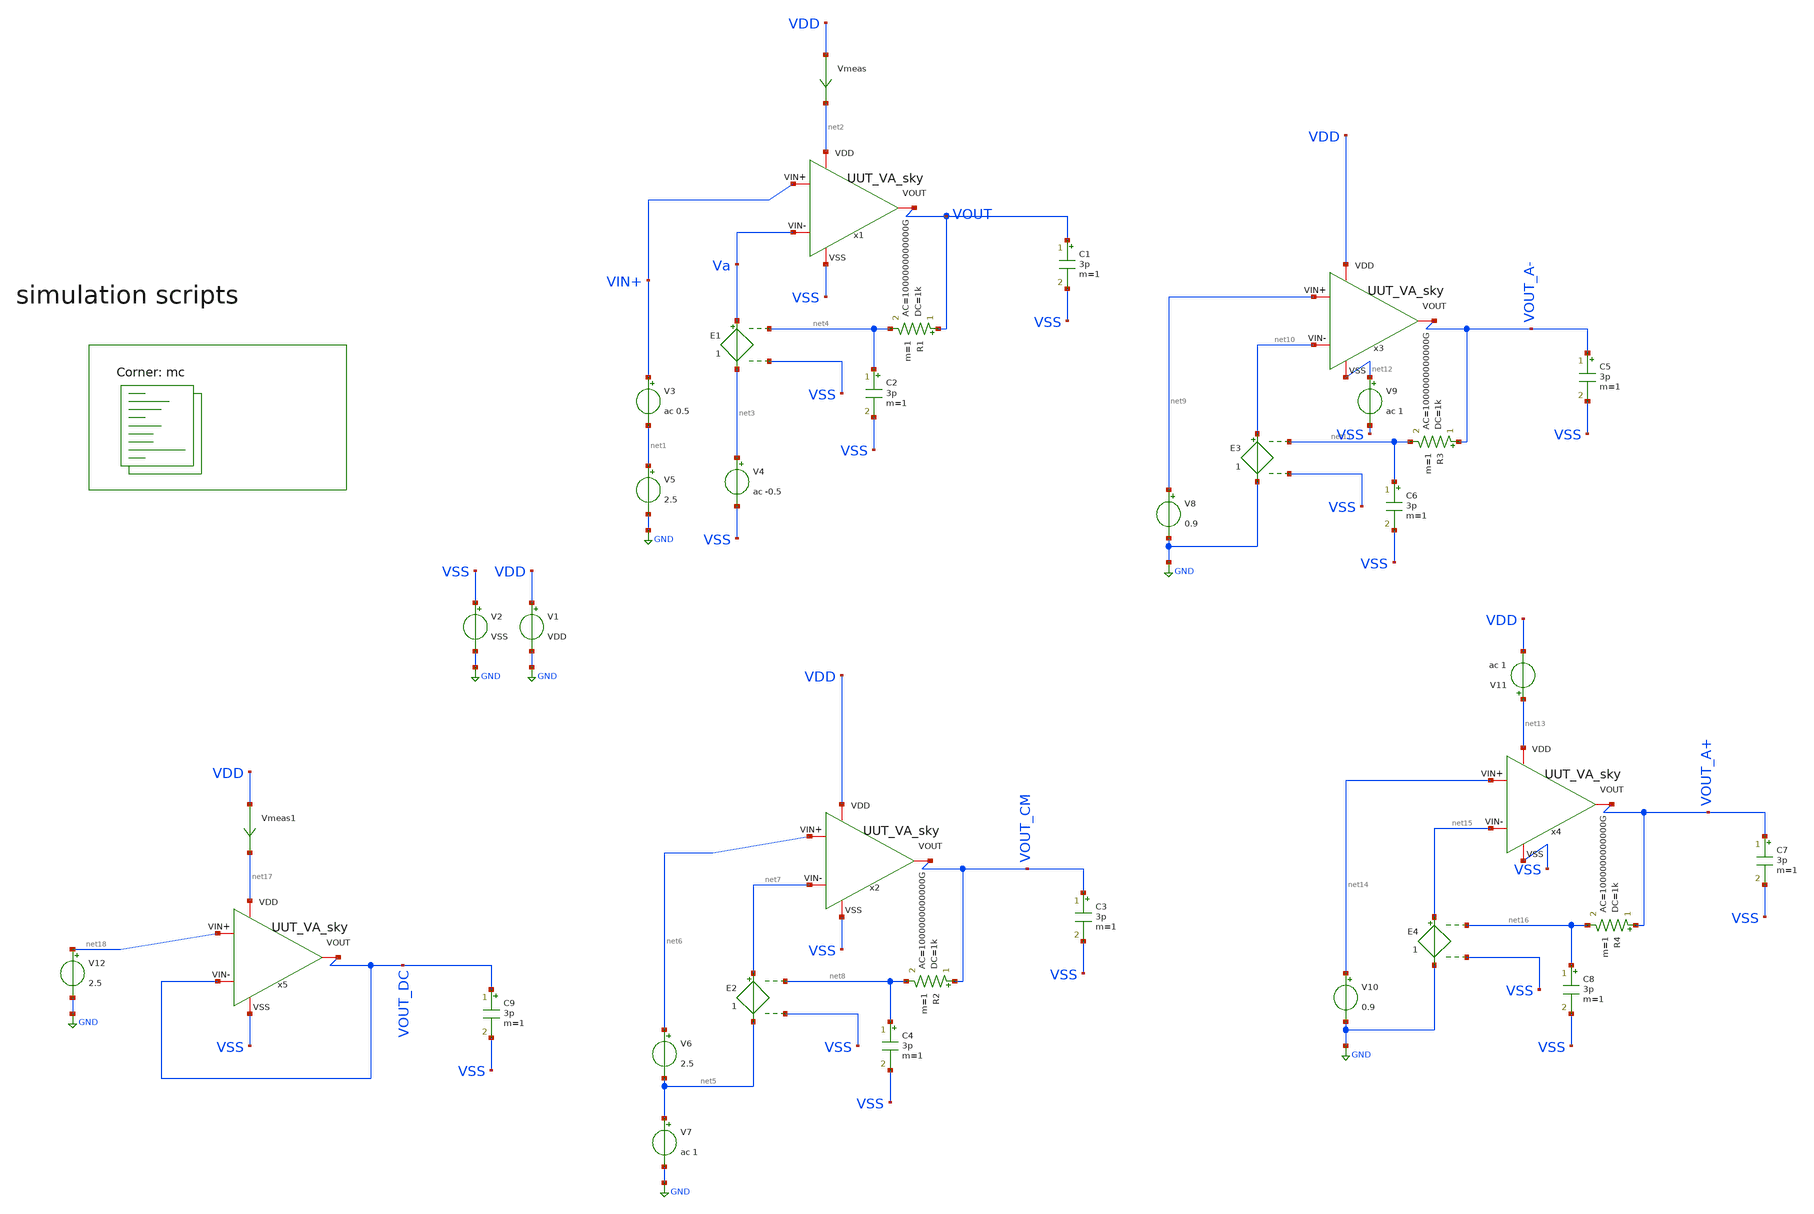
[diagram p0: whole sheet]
** sch_path: Learning/single_ended_amplifiers/Design_and_Analysis_of_Two-Stage_CMOS_Operational_Amplifier_for_Fluorescence_Signal_Processing_sky130_5V/amplifier_design/OTA_mc_tb.sch
**.subckt OTA_mc_tb
V1 VDD GND VDD
V2 VSS GND VSS
Vmeas VDD net2 0
.save i(vmeas)
x1 net2 VSS Va VIN+ VOUT UUT_VA_sky
C1 VOUT VSS 3p m=1
V5 net1 GND 2.5
V3 VIN+ net1 ac 0.5
V4 net3 VSS ac -0.5
E1 Va net3 net4 VSS 1
R1 VOUT net4 1k ac=1000000000000G m=1
C2 net4 VSS 3p m=1
x2 VDD VSS net7 net6 VOUT_CM UUT_VA_sky
C3 VOUT_CM VSS 3p m=1
V6 net6 net5 2.5
V7 net5 GND ac 1
E2 net7 net5 net8 VSS 1
R2 VOUT_CM net8 1k ac=1000000000000G m=1
C4 net8 VSS 3p m=1
x3 VDD net12 net10 net9 VOUT_A- UUT_VA_sky
C5 VOUT_A- VSS 3p m=1
V8 net9 GND 0.9
E3 net10 GND net11 VSS 1
R3 VOUT_A- net11 1k ac=1000000000000G m=1
C6 net11 VSS 3p m=1
V9 net12 VSS ac 1
x4 net13 VSS net15 net14 VOUT_A+ UUT_VA_sky
C7 VOUT_A+ VSS 3p m=1
V10 net14 GND 0.9
E4 net15 GND net16 VSS 1
R4 VOUT_A+ net16 1k ac=1000000000000G m=1
C8 net16 VSS 3p m=1
V11 net13 VDD ac 1
Vmeas1 VDD net17 0
.save i(vmeas1)
x5 net17 VSS VOUT_DC net18 VOUT_DC UUT_VA_sky
C9 VOUT_DC VSS 3p m=1
V12 net18 GND 2.5
**** begin user architecture code
.lib $::SKYWATER_MODELS/sky130.lib.spice mc

.Temp 27
.param VDD = 5
.param VSS = 0
.param CL = 3p


.control

	save all
	dc V12 0 1.8 0.001
	plot v(VOUT_DC)
	ac dec 100 1 10G
	plot db(v(VOUT))
	plot db(v(VOUT_CM))
	plot db(v(VOUT_A-))
	plot db(v(VOUT_A+))
.endc


.subckt A001 VDD VSS Vin+ Vin- VOUT
X0 bias_res_0/li_3970_7618# bias_res_0/li_2816_7756# VSS sky130_fd_pr__res_high_po_0p69 l=1.57
X1 VSS VSS VSS sky130_fd_pr__res_high_po_0p69 l=1.57
X2 bias_res_0/li_3970_7364# Lower_Nmos_0/IC VSS sky130_fd_pr__res_high_po_0p69 l=1.57
X3 bias_res_0/li_3970_7872# bias_res_0/li_2816_7756# VSS sky130_fd_pr__res_high_po_0p69 l=1.57
X4 VSS VSS VSS sky130_fd_pr__res_high_po_0p69 l=1.57
X5 bias_res_0/li_3970_8126# bias_res_0/li_2816_8248# VSS sky130_fd_pr__res_high_po_0p69 l=1.57
X6 bias_res_0/li_3969_8380# bias_res_0/li_2816_8248# VSS sky130_fd_pr__res_high_po_0p69 l=1.57
X7 VSS VSS VSS sky130_fd_pr__res_high_po_0p69 l=2.72
X8 VSS VSS VSS sky130_fd_pr__res_high_po_0p69 l=2.72
X9 bias_res_0/li_5323_7502# bias_res_0/li_3970_7364# VSS sky130_fd_pr__res_high_po_0p69 l=2.72
X10 bias_res_0/li_5323_7502# bias_res_0/li_3970_7618# VSS sky130_fd_pr__res_high_po_0p69 l=2.72
X11 bias_res_0/li_5321_8010# bias_res_0/li_3970_7872# VSS sky130_fd_pr__res_high_po_0p69 l=2.72
X12 bias_res_0/li_5321_8010# bias_res_0/li_3970_8126# VSS sky130_fd_pr__res_high_po_0p69 l=2.72
X13 VSS bias_res_0/li_3969_8380# VSS sky130_fd_pr__res_high_po_0p69 l=2.72
X14 VOUT VSS VSS VSS sky130_fd_pr__nfet_g5v0d10v5 ad=1 pd=4.5 as=1.2 ps=8.6 w=4 l=1
X15 VSS active_load_0/IA VOUT VSS sky130_fd_pr__nfet_g5v0d10v5 ad=1 pd=4.5 as=1 ps=4.5 w=4 l=1
X16 VSS VSS VOUT VSS sky130_fd_pr__nfet_g5v0d10v5 ad=1.2 pd=8.6 as=1 ps=4.5 w=4 l=1
X17 VOUT active_load_0/IA VSS VSS sky130_fd_pr__nfet_g5v0d10v5 ad=1 pd=4.5 as=1 ps=4.5 w=4 l=1
X18 VOUT VSS VSS VSS sky130_fd_pr__nfet_g5v0d10v5 ad=8 pd=36 as=20 ps=127.6 w=4 l=1
X19 VSS active_load_0/IA VOUT VSS sky130_fd_pr__nfet_g5v0d10v5 ad=0 pd=0 as=0 ps=0 w=4 l=1
X20 VSS VSS VOUT VSS sky130_fd_pr__nfet_g5v0d10v5 ad=0 pd=0 as=0 ps=0 w=4 l=1
X21 VOUT active_load_0/IA VSS VSS sky130_fd_pr__nfet_g5v0d10v5 ad=0 pd=0 as=0 ps=0 w=4 l=1
X22 VSS active_load_0/IB active_load_0/IA VSS sky130_fd_pr__nfet_g5v0d10v5 ad=0.375 pd=2 as=0.375
+ ps=2 w=1.5 l=2
X23 active_load_0/IB VSS VSS VSS sky130_fd_pr__nfet_g5v0d10v5 ad=0.375 pd=2 as=0.45 ps=3.6 w=1.5 l=2
X24 active_load_0/IA active_load_0/IB VSS VSS sky130_fd_pr__nfet_g5v0d10v5 ad=0.375 pd=2 as=0.375
+ ps=2 w=1.5 l=2
X25 VSS active_load_0/IB active_load_0/IB VSS sky130_fd_pr__nfet_g5v0d10v5 ad=0.375 pd=2 as=0.375
+ ps=2 w=1.5 l=2
X26 VSS VSS active_load_0/IB VSS sky130_fd_pr__nfet_g5v0d10v5 ad=0.45 pd=3.6 as=0.375 ps=2 w=1.5 l=2
X27 active_load_0/IB active_load_0/IB VSS VSS sky130_fd_pr__nfet_g5v0d10v5 ad=0.375 pd=2 as=0.375
+ ps=2 w=1.5 l=2
X28 VSS active_load_0/IB active_load_0/IA VSS sky130_fd_pr__nfet_g5v0d10v5 ad=0 pd=0 as=2.34 ps=14.8
+ w=1.5 l=2
X29 active_load_0/IB VSS VSS VSS sky130_fd_pr__nfet_g5v0d10v5 ad=3 pd=16 as=0 ps=0 w=1.5 l=2
X30 active_load_0/IA active_load_0/IB VSS VSS sky130_fd_pr__nfet_g5v0d10v5 ad=0 pd=0 as=0 ps=0 w=1.5
+ l=2
X31 VSS active_load_0/IB active_load_0/IB VSS sky130_fd_pr__nfet_g5v0d10v5 ad=0 pd=0 as=0 ps=0 w=1.5
+ l=2
X32 VSS VSS active_load_0/IB VSS sky130_fd_pr__nfet_g5v0d10v5 ad=0 pd=0 as=0 ps=0 w=1.5 l=2
X33 active_load_0/IB active_load_0/IB VSS VSS sky130_fd_pr__nfet_g5v0d10v5 ad=0 pd=0 as=0 ps=0 w=1.5
+ l=2
X34 active_load_0/IA Vin+ Pmos_current_mirror_0/IC Pmos_current_mirror_0/IC
+ sky130_fd_pr__pfet_g5v0d10v5 ad=1.125 pd=5 as=1.125 ps=5 w=4.5 l=1
X35 active_load_0/IB Vin- Pmos_current_mirror_0/IC Pmos_current_mirror_0/IC
+ sky130_fd_pr__pfet_g5v0d10v5 ad=1.125 pd=5 as=1.125 ps=5 w=4.5 l=1
X36 Pmos_current_mirror_0/IC Pmos_current_mirror_0/IC Pmos_current_mirror_0/IC
+ Pmos_current_mirror_0/IC sky130_fd_pr__pfet_g5v0d10v5 ad=1.125 pd=5 as=1.35 ps=9.6 w=4.5 l=1
X37 Pmos_current_mirror_0/IC Pmos_current_mirror_0/IC Pmos_current_mirror_0/IC
+ Pmos_current_mirror_0/IC sky130_fd_pr__pfet_g5v0d10v5 ad=1.35 pd=9.6 as=1.125 ps=5 w=4.5 l=1
X38 active_load_0/IB Vin- Pmos_current_mirror_0/IC Pmos_current_mirror_0/IC
+ sky130_fd_pr__pfet_g5v0d10v5 ad=1.125 pd=5 as=1.125 ps=5 w=4.5 l=1
X39 active_load_0/IA Vin+ Pmos_current_mirror_0/IC Pmos_current_mirror_0/IC
+ sky130_fd_pr__pfet_g5v0d10v5 ad=1.125 pd=5 as=1.125 ps=5 w=4.5 l=1
X40 Pmos_current_mirror_0/IC Vin+ active_load_0/IA Pmos_current_mirror_0/IC
+ sky130_fd_pr__pfet_g5v0d10v5 ad=1.125 pd=5 as=1.125 ps=5 w=4.5 l=1
X41 Pmos_current_mirror_0/IC Vin+ active_load_0/IA Pmos_current_mirror_0/IC
+ sky130_fd_pr__pfet_g5v0d10v5 ad=1.125 pd=5 as=1.125 ps=5 w=4.5 l=1
X42 Pmos_current_mirror_0/IC Vin- active_load_0/IB Pmos_current_mirror_0/IC
+ sky130_fd_pr__pfet_g5v0d10v5 ad=1.125 pd=5 as=1.125 ps=5 w=4.5 l=1
X43 Pmos_current_mirror_0/IC Vin- active_load_0/IB Pmos_current_mirror_0/IC
+ sky130_fd_pr__pfet_g5v0d10v5 ad=1.125 pd=5 as=1.125 ps=5 w=4.5 l=1
X44 active_load_0/IB Vin- Pmos_current_mirror_0/IC Pmos_current_mirror_0/IC
+ sky130_fd_pr__pfet_g5v0d10v5 ad=9 pd=40 as=31.9 ps=162.39999 w=4.5 l=1
X45 active_load_0/IA Vin+ Pmos_current_mirror_0/IC Pmos_current_mirror_0/IC
+ sky130_fd_pr__pfet_g5v0d10v5 ad=9 pd=40 as=0 ps=0 w=4.5 l=1
X46 Pmos_current_mirror_0/IC Pmos_current_mirror_0/IC Pmos_current_mirror_0/IC
+ Pmos_current_mirror_0/IC sky130_fd_pr__pfet_g5v0d10v5 ad=0 pd=0 as=0 ps=0 w=4.5 l=1
X47 Pmos_current_mirror_0/IC Pmos_current_mirror_0/IC Pmos_current_mirror_0/IC
+ Pmos_current_mirror_0/IC sky130_fd_pr__pfet_g5v0d10v5 ad=0 pd=0 as=0 ps=0 w=4.5 l=1
X48 active_load_0/IA Vin+ Pmos_current_mirror_0/IC Pmos_current_mirror_0/IC
+ sky130_fd_pr__pfet_g5v0d10v5 ad=0 pd=0 as=0 ps=0 w=4.5 l=1
X49 active_load_0/IB Vin- Pmos_current_mirror_0/IC Pmos_current_mirror_0/IC
+ sky130_fd_pr__pfet_g5v0d10v5 ad=0 pd=0 as=0 ps=0 w=4.5 l=1
X50 Pmos_current_mirror_0/IC Vin- active_load_0/IB Pmos_current_mirror_0/IC
+ sky130_fd_pr__pfet_g5v0d10v5 ad=0 pd=0 as=0 ps=0 w=4.5 l=1
X51 Pmos_current_mirror_0/IC Vin- active_load_0/IB Pmos_current_mirror_0/IC
+ sky130_fd_pr__pfet_g5v0d10v5 ad=0 pd=0 as=0 ps=0 w=4.5 l=1
X52 Pmos_current_mirror_0/IC Vin+ active_load_0/IA Pmos_current_mirror_0/IC
+ sky130_fd_pr__pfet_g5v0d10v5 ad=0 pd=0 as=0 ps=0 w=4.5 l=1
X53 Pmos_current_mirror_0/IC Vin+ active_load_0/IA Pmos_current_mirror_0/IC
+ sky130_fd_pr__pfet_g5v0d10v5 ad=0 pd=0 as=0 ps=0 w=4.5 l=1
X54 VDD Pmos_current_mirror_0/IA Pmos_current_mirror_0/IA VDD sky130_fd_pr__pfet_g5v0d10v5 ad=0.25
+ pd=1.5 as=0.25 ps=1.5 w=1 l=2.2
X55 VDD Pmos_current_mirror_0/IA VOUT VDD sky130_fd_pr__pfet_g5v0d10v5 ad=0.25 pd=1.5 as=0.25 ps=1.5
+ w=1 l=2.2
X56 Pmos_current_mirror_0/IA VDD VDD VDD sky130_fd_pr__pfet_g5v0d10v5 ad=0.25 pd=1.5 as=0.3 ps=2.6
+ w=1 l=2.2
X57 VOUT Pmos_current_mirror_0/IA VDD VDD sky130_fd_pr__pfet_g5v0d10v5 ad=0.25 pd=1.5 as=0.25 ps=1.5
+ w=1 l=2.2
X58 Pmos_current_mirror_0/IC Pmos_current_mirror_0/IA VDD VDD sky130_fd_pr__pfet_g5v0d10v5 ad=0.25
+ pd=1.5 as=0.25 ps=1.5 w=1 l=2.2
X59 VDD Pmos_current_mirror_0/IA Pmos_current_mirror_0/IB VDD sky130_fd_pr__pfet_g5v0d10v5 ad=0.25
+ pd=1.5 as=0.25 ps=1.5 w=1 l=2.2
X60 VDD VDD Pmos_current_mirror_0/IA VDD sky130_fd_pr__pfet_g5v0d10v5 ad=0.25 pd=1.5 as=0.25 ps=1.5
+ w=1 l=2.2
X61 VDD Pmos_current_mirror_0/IA Pmos_current_mirror_0/IC VDD sky130_fd_pr__pfet_g5v0d10v5 ad=0.25
+ pd=1.5 as=0.25 ps=1.5 w=1 l=2.2
X62 VDD Pmos_current_mirror_0/IA Pmos_current_mirror_0/IC VDD sky130_fd_pr__pfet_g5v0d10v5 ad=0.25
+ pd=1.5 as=0.25 ps=1.5 w=1 l=2.2
X63 VOUT Pmos_current_mirror_0/IA VDD VDD sky130_fd_pr__pfet_g5v0d10v5 ad=0.25 pd=1.5 as=0.25 ps=1.5
+ w=1 l=2.2
X64 VOUT Pmos_current_mirror_0/IA VDD VDD sky130_fd_pr__pfet_g5v0d10v5 ad=0.25 pd=1.5 as=0.25 ps=1.5
+ w=1 l=2.2
X65 VOUT Pmos_current_mirror_0/IA VDD VDD sky130_fd_pr__pfet_g5v0d10v5 ad=0.25 pd=1.5 as=0.25 ps=1.5
+ w=1 l=2.2
X66 Pmos_current_mirror_0/IB Pmos_current_mirror_0/IA VDD VDD sky130_fd_pr__pfet_g5v0d10v5 ad=0.25
+ pd=1.5 as=0.25 ps=1.5 w=1 l=2.2
X67 Pmos_current_mirror_0/IA Pmos_current_mirror_0/IA VDD VDD sky130_fd_pr__pfet_g5v0d10v5 ad=0.25
+ pd=1.5 as=0.25 ps=1.5 w=1 l=2.2
X68 Pmos_current_mirror_0/IC Pmos_current_mirror_0/IA VDD VDD sky130_fd_pr__pfet_g5v0d10v5 ad=0.25
+ pd=1.5 as=0.25 ps=1.5 w=1 l=2.2
X69 VDD Pmos_current_mirror_0/IA VOUT VDD sky130_fd_pr__pfet_g5v0d10v5 ad=0.25 pd=1.5 as=0.25 ps=1.5
+ w=1 l=2.2
X70 VDD Pmos_current_mirror_0/IA VOUT VDD sky130_fd_pr__pfet_g5v0d10v5 ad=0.25 pd=1.5 as=0.25 ps=1.5
+ w=1 l=2.2
X71 VDD Pmos_current_mirror_0/IA VOUT VDD sky130_fd_pr__pfet_g5v0d10v5 ad=0.25 pd=1.5 as=0.25 ps=1.5
+ w=1 l=2.2
X72 VDD Pmos_current_mirror_0/IA VOUT VDD sky130_fd_pr__pfet_g5v0d10v5 ad=0.25 pd=1.5 as=0.25 ps=1.5
+ w=1 l=2.2
X73 VDD Pmos_current_mirror_0/IA VOUT VDD sky130_fd_pr__pfet_g5v0d10v5 ad=0.25 pd=1.5 as=0.25 ps=1.5
+ w=1 l=2.2
X74 Pmos_current_mirror_0/IC Pmos_current_mirror_0/IA VDD VDD sky130_fd_pr__pfet_g5v0d10v5 ad=0.25
+ pd=1.5 as=0.25 ps=1.5 w=1 l=2.2
X75 VDD VDD VDD VDD sky130_fd_pr__pfet_g5v0d10v5 ad=0.3 pd=2.6 as=0.25 ps=1.5 w=1 l=2.2
X76 Pmos_current_mirror_0/IC Pmos_current_mirror_0/IA VDD VDD sky130_fd_pr__pfet_g5v0d10v5 ad=0.25
+ pd=1.5 as=0.25 ps=1.5 w=1 l=2.2
X77 VOUT Pmos_current_mirror_0/IA VDD VDD sky130_fd_pr__pfet_g5v0d10v5 ad=0.25 pd=1.5 as=0.25 ps=1.5
+ w=1 l=2.2
X78 VOUT Pmos_current_mirror_0/IA VDD VDD sky130_fd_pr__pfet_g5v0d10v5 ad=0.25 pd=1.5 as=0.25 ps=1.5
+ w=1 l=2.2
X79 VOUT Pmos_current_mirror_0/IA VDD VDD sky130_fd_pr__pfet_g5v0d10v5 ad=0.25 pd=1.5 as=0.25 ps=1.5
+ w=1 l=2.2
X80 VOUT Pmos_current_mirror_0/IA VDD VDD sky130_fd_pr__pfet_g5v0d10v5 ad=0.25 pd=1.5 as=0.25 ps=1.5
+ w=1 l=2.2
X81 VDD Pmos_current_mirror_0/IA VOUT VDD sky130_fd_pr__pfet_g5v0d10v5 ad=0.25 pd=1.5 as=0.25 ps=1.5
+ w=1 l=2.2
X82 VDD Pmos_current_mirror_0/IA VOUT VDD sky130_fd_pr__pfet_g5v0d10v5 ad=0.25 pd=1.5 as=0.25 ps=1.5
+ w=1 l=2.2
X83 VDD Pmos_current_mirror_0/IA Pmos_current_mirror_0/IC VDD sky130_fd_pr__pfet_g5v0d10v5 ad=0.25
+ pd=1.5 as=0.25 ps=1.5 w=1 l=2.2
X84 VDD Pmos_current_mirror_0/IA Pmos_current_mirror_0/IC VDD sky130_fd_pr__pfet_g5v0d10v5 ad=0.25
+ pd=1.5 as=0.25 ps=1.5 w=1 l=2.2
X85 VDD Pmos_current_mirror_0/IA Pmos_current_mirror_0/IA VDD sky130_fd_pr__pfet_g5v0d10v5 ad=16.2
+ pd=100.4 as=2 ps=12 w=1 l=2.2
X86 VDD Pmos_current_mirror_0/IA VOUT VDD sky130_fd_pr__pfet_g5v0d10v5 ad=0 pd=0 as=8 ps=48 w=1
+ l=2.2
X87 Pmos_current_mirror_0/IA VDD VDD VDD sky130_fd_pr__pfet_g5v0d10v5 ad=0 pd=0 as=0 ps=0 w=1 l=2.2
X88 VOUT Pmos_current_mirror_0/IA VDD VDD sky130_fd_pr__pfet_g5v0d10v5 ad=0 pd=0 as=0 ps=0 w=1 l=2.2
X89 Pmos_current_mirror_0/IC Pmos_current_mirror_0/IA VDD VDD sky130_fd_pr__pfet_g5v0d10v5 ad=0 pd=0
+ as=0 ps=0 w=1 l=2.2
X90 VDD Pmos_current_mirror_0/IA Pmos_current_mirror_0/IB VDD sky130_fd_pr__pfet_g5v0d10v5 ad=0 pd=0
+ as=1 ps=6 w=1 l=2.2
X91 VDD VDD Pmos_current_mirror_0/IA VDD sky130_fd_pr__pfet_g5v0d10v5 ad=0 pd=0 as=0 ps=0 w=1 l=2.2
X92 VDD Pmos_current_mirror_0/IA Pmos_current_mirror_0/IC VDD sky130_fd_pr__pfet_g5v0d10v5 ad=0 pd=0
+ as=0 ps=0 w=1 l=2.2
X93 VDD Pmos_current_mirror_0/IA Pmos_current_mirror_0/IC VDD sky130_fd_pr__pfet_g5v0d10v5 ad=0 pd=0
+ as=0 ps=0 w=1 l=2.2
X94 VOUT Pmos_current_mirror_0/IA VDD VDD sky130_fd_pr__pfet_g5v0d10v5 ad=0 pd=0 as=0 ps=0 w=1 l=2.2
X95 VOUT Pmos_current_mirror_0/IA VDD VDD sky130_fd_pr__pfet_g5v0d10v5 ad=0 pd=0 as=0 ps=0 w=1 l=2.2
X96 VOUT Pmos_current_mirror_0/IA VDD VDD sky130_fd_pr__pfet_g5v0d10v5 ad=0 pd=0 as=0 ps=0 w=1 l=2.2
X97 Pmos_current_mirror_0/IB Pmos_current_mirror_0/IA VDD VDD sky130_fd_pr__pfet_g5v0d10v5 ad=0 pd=0
+ as=0 ps=0 w=1 l=2.2
X98 Pmos_current_mirror_0/IA Pmos_current_mirror_0/IA VDD VDD sky130_fd_pr__pfet_g5v0d10v5 ad=0 pd=0
+ as=0 ps=0 w=1 l=2.2
X99 Pmos_current_mirror_0/IC Pmos_current_mirror_0/IA VDD VDD sky130_fd_pr__pfet_g5v0d10v5 ad=0 pd=0
+ as=0 ps=0 w=1 l=2.2
X100 VDD Pmos_current_mirror_0/IA VOUT VDD sky130_fd_pr__pfet_g5v0d10v5 ad=0 pd=0 as=0 ps=0 w=1
+ l=2.2
X101 VDD Pmos_current_mirror_0/IA VOUT VDD sky130_fd_pr__pfet_g5v0d10v5 ad=0 pd=0 as=0 ps=0 w=1
+ l=2.2
X102 VDD Pmos_current_mirror_0/IA VOUT VDD sky130_fd_pr__pfet_g5v0d10v5 ad=0 pd=0 as=0 ps=0 w=1
+ l=2.2
X103 VDD Pmos_current_mirror_0/IA VOUT VDD sky130_fd_pr__pfet_g5v0d10v5 ad=0 pd=0 as=0 ps=0 w=1
+ l=2.2
X104 VDD Pmos_current_mirror_0/IA VOUT VDD sky130_fd_pr__pfet_g5v0d10v5 ad=0 pd=0 as=0 ps=0 w=1
+ l=2.2
X105 Pmos_current_mirror_0/IC Pmos_current_mirror_0/IA VDD VDD sky130_fd_pr__pfet_g5v0d10v5 ad=0
+ pd=0 as=0 ps=0 w=1 l=2.2
X106 VDD VDD VDD VDD sky130_fd_pr__pfet_g5v0d10v5 ad=0 pd=0 as=0 ps=0 w=1 l=2.2
X107 Pmos_current_mirror_0/IC Pmos_current_mirror_0/IA VDD VDD sky130_fd_pr__pfet_g5v0d10v5 ad=0
+ pd=0 as=0 ps=0 w=1 l=2.2
X108 VOUT Pmos_current_mirror_0/IA VDD VDD sky130_fd_pr__pfet_g5v0d10v5 ad=0 pd=0 as=0 ps=0 w=1
+ l=2.2
X109 VOUT Pmos_current_mirror_0/IA VDD VDD sky130_fd_pr__pfet_g5v0d10v5 ad=0 pd=0 as=0 ps=0 w=1
+ l=2.2
X110 VOUT Pmos_current_mirror_0/IA VDD VDD sky130_fd_pr__pfet_g5v0d10v5 ad=0 pd=0 as=0 ps=0 w=1
+ l=2.2
X111 VOUT Pmos_current_mirror_0/IA VDD VDD sky130_fd_pr__pfet_g5v0d10v5 ad=0 pd=0 as=0 ps=0 w=1
+ l=2.2
X112 VDD Pmos_current_mirror_0/IA VOUT VDD sky130_fd_pr__pfet_g5v0d10v5 ad=0 pd=0 as=0 ps=0 w=1
+ l=2.2
X113 VDD Pmos_current_mirror_0/IA VOUT VDD sky130_fd_pr__pfet_g5v0d10v5 ad=0 pd=0 as=0 ps=0 w=1
+ l=2.2
X114 VDD Pmos_current_mirror_0/IA Pmos_current_mirror_0/IC VDD sky130_fd_pr__pfet_g5v0d10v5 ad=0
+ pd=0 as=0 ps=0 w=1 l=2.2
X115 VDD Pmos_current_mirror_0/IA Pmos_current_mirror_0/IC VDD sky130_fd_pr__pfet_g5v0d10v5 ad=0
+ pd=0 as=0 ps=0 w=1 l=2.2
X116 m1_17410_n5244# Pmos_current_mirror_0/IB active_load_0/IA VSS sky130_fd_pr__nfet_g5v0d10v5
+ ad=0.35 pd=1.9 as=0.42 ps=3.4 w=1.4 l=2.6
X117 active_load_0/IA Pmos_current_mirror_0/IB m1_17410_n5244# VSS sky130_fd_pr__nfet_g5v0d10v5
+ ad=0.42 pd=3.4 as=0.35 ps=1.9 w=1.4 l=2.6
X118 Pmos_current_mirror_0/IA VSS VSS VSS sky130_fd_pr__nfet_g5v0d10v5 ad=0.25 pd=1.5 as=0.25 ps=1.5
+ w=1 l=2
X119 Pmos_current_mirror_0/IB VSS VSS VSS sky130_fd_pr__nfet_g5v0d10v5 ad=0.25 pd=1.5 as=0.3 ps=2.6
+ w=1 l=2
X120 VSS VSS Lower_Nmos_0/IA VSS sky130_fd_pr__nfet_g5v0d10v5 ad=0.25 pd=1.5 as=0.25 ps=1.5 w=1 l=2
X121 VSS VSS Pmos_current_mirror_0/IB VSS sky130_fd_pr__nfet_g5v0d10v5 ad=0.3 pd=2.6 as=0.25 ps=1.5
+ w=1 l=2
X122 Pmos_current_mirror_0/IB Pmos_current_mirror_0/IB Lower_Nmos_0/IA VSS
+ sky130_fd_pr__nfet_g5v0d10v5 ad=0.25 pd=1.5 as=0.25 ps=1.5 w=1 l=2
X123 Lower_Nmos_0/IA VSS VSS VSS sky130_fd_pr__nfet_g5v0d10v5 ad=0.25 pd=1.5 as=0.25 ps=1.5 w=1 l=2
X124 Lower_Nmos_0/IA Pmos_current_mirror_0/IB Pmos_current_mirror_0/IB VSS
+ sky130_fd_pr__nfet_g5v0d10v5 ad=0.25 pd=1.5 as=0.25 ps=1.5 w=1 l=2
X125 VSS VSS Pmos_current_mirror_0/IA VSS sky130_fd_pr__nfet_g5v0d10v5 ad=0.25 pd=1.5 as=0.25 ps=1.5
+ w=1 l=2
X126 Pmos_current_mirror_0/IA Pmos_current_mirror_0/IB Lower_Nmos_0/IB VSS
+ sky130_fd_pr__nfet_g5v0d10v5 ad=0.25 pd=1.5 as=0.25 ps=1.5 w=1 l=2
X127 Lower_Nmos_0/IB Pmos_current_mirror_0/IB Pmos_current_mirror_0/IA VSS
+ sky130_fd_pr__nfet_g5v0d10v5 ad=0.25 pd=1.5 as=0.25 ps=1.5 w=1 l=2
X128 Pmos_current_mirror_0/IA VSS VSS VSS sky130_fd_pr__nfet_g5v0d10v5 ad=2 pd=12 as=0 ps=0 w=1 l=2
X129 Pmos_current_mirror_0/IB VSS VSS VSS sky130_fd_pr__nfet_g5v0d10v5 ad=2 pd=12 as=0 ps=0 w=1 l=2
X130 VSS VSS Lower_Nmos_0/IA VSS sky130_fd_pr__nfet_g5v0d10v5 ad=0 pd=0 as=4 ps=24 w=1 l=2
X131 VSS VSS Pmos_current_mirror_0/IB VSS sky130_fd_pr__nfet_g5v0d10v5 ad=0 pd=0 as=0 ps=0 w=1 l=2
X132 Pmos_current_mirror_0/IB Pmos_current_mirror_0/IB Lower_Nmos_0/IA VSS
+ sky130_fd_pr__nfet_g5v0d10v5 ad=0 pd=0 as=0 ps=0 w=1 l=2
X133 Lower_Nmos_0/IA VSS VSS VSS sky130_fd_pr__nfet_g5v0d10v5 ad=0 pd=0 as=0 ps=0 w=1 l=2
X134 Lower_Nmos_0/IA Pmos_current_mirror_0/IB Pmos_current_mirror_0/IB VSS
+ sky130_fd_pr__nfet_g5v0d10v5 ad=0 pd=0 as=0 ps=0 w=1 l=2
X135 VSS VSS Pmos_current_mirror_0/IA VSS sky130_fd_pr__nfet_g5v0d10v5 ad=0 pd=0 as=0 ps=0 w=1 l=2
X136 Pmos_current_mirror_0/IA Pmos_current_mirror_0/IB Lower_Nmos_0/IB VSS
+ sky130_fd_pr__nfet_g5v0d10v5 ad=0 pd=0 as=6 ps=36 w=1 l=2
X137 Lower_Nmos_0/IB Pmos_current_mirror_0/IB Pmos_current_mirror_0/IA VSS
+ sky130_fd_pr__nfet_g5v0d10v5 ad=0 pd=0 as=0 ps=0 w=1 l=2
X138 Lower_Nmos_0/IA Lower_Nmos_0/IA VSS VSS sky130_fd_pr__nfet_g5v0d10v5 ad=0.25 pd=1.5 as=0.25
+ ps=1.5 w=1 l=3.2
X139 Lower_Nmos_0/IA VSS VSS VSS sky130_fd_pr__nfet_g5v0d10v5 ad=0.25 pd=1.5 as=0.3 ps=2.6 w=1 l=3.2
X140 Lower_Nmos_0/IB VSS VSS VSS sky130_fd_pr__nfet_g5v0d10v5 ad=0.25 pd=1.5 as=0.25 ps=1.5 w=1
+ l=3.2
X141 VSS VSS Lower_Nmos_0/IA VSS sky130_fd_pr__nfet_g5v0d10v5 ad=0.3 pd=2.6 as=0.25 ps=1.5 w=1 l=3.2
X142 Lower_Nmos_0/IC Lower_Nmos_0/IA Lower_Nmos_0/IB VSS sky130_fd_pr__nfet_g5v0d10v5 ad=0.25 pd=1.5
+ as=0.25 ps=1.5 w=1 l=3.2
X143 Lower_Nmos_0/IC Lower_Nmos_0/IA Lower_Nmos_0/IB VSS sky130_fd_pr__nfet_g5v0d10v5 ad=0.25 pd=1.5
+ as=0.25 ps=1.5 w=1 l=3.2
X144 VSS Lower_Nmos_0/IA Lower_Nmos_0/IA VSS sky130_fd_pr__nfet_g5v0d10v5 ad=0.25 pd=1.5 as=0.25
+ ps=1.5 w=1 l=3.2
X145 Lower_Nmos_0/IB Lower_Nmos_0/IA Lower_Nmos_0/IC VSS sky130_fd_pr__nfet_g5v0d10v5 ad=0.25 pd=1.5
+ as=0.25 ps=1.5 w=1 l=3.2
X146 Lower_Nmos_0/IB Lower_Nmos_0/IA Lower_Nmos_0/IC VSS sky130_fd_pr__nfet_g5v0d10v5 ad=0.25 pd=1.5
+ as=0.25 ps=1.5 w=1 l=3.2
X147 Lower_Nmos_0/IC Lower_Nmos_0/IA Lower_Nmos_0/IB VSS sky130_fd_pr__nfet_g5v0d10v5 ad=0.25 pd=1.5
+ as=0.25 ps=1.5 w=1 l=3.2
X148 Lower_Nmos_0/IB Lower_Nmos_0/IA Lower_Nmos_0/IC VSS sky130_fd_pr__nfet_g5v0d10v5 ad=0.25 pd=1.5
+ as=0.25 ps=1.5 w=1 l=3.2
X149 Lower_Nmos_0/IB Lower_Nmos_0/IA Lower_Nmos_0/IC VSS sky130_fd_pr__nfet_g5v0d10v5 ad=0.25 pd=1.5
+ as=0.25 ps=1.5 w=1 l=3.2
X150 Lower_Nmos_0/IC Lower_Nmos_0/IA Lower_Nmos_0/IB VSS sky130_fd_pr__nfet_g5v0d10v5 ad=0.25 pd=1.5
+ as=0.25 ps=1.5 w=1 l=3.2
X151 VSS VSS Lower_Nmos_0/IB VSS sky130_fd_pr__nfet_g5v0d10v5 ad=0.25 pd=1.5 as=0.25 ps=1.5 w=1
+ l=3.2
X152 Lower_Nmos_0/IA Lower_Nmos_0/IA VSS VSS sky130_fd_pr__nfet_g5v0d10v5 ad=0.25 pd=1.5 as=0.25
+ ps=1.5 w=1 l=3.2
X153 Lower_Nmos_0/IA VSS VSS VSS sky130_fd_pr__nfet_g5v0d10v5 ad=0.25 pd=1.5 as=0.3 ps=2.6 w=1 l=3.2
X154 Lower_Nmos_0/IB VSS VSS VSS sky130_fd_pr__nfet_g5v0d10v5 ad=0.25 pd=1.5 as=0.25 ps=1.5 w=1
+ l=3.2
X155 VSS VSS Lower_Nmos_0/IA VSS sky130_fd_pr__nfet_g5v0d10v5 ad=0.3 pd=2.6 as=0.25 ps=1.5 w=1 l=3.2
X156 Lower_Nmos_0/IC Lower_Nmos_0/IA Lower_Nmos_0/IB VSS sky130_fd_pr__nfet_g5v0d10v5 ad=0.25 pd=1.5
+ as=0.25 ps=1.5 w=1 l=3.2
X157 Lower_Nmos_0/IC Lower_Nmos_0/IA Lower_Nmos_0/IB VSS sky130_fd_pr__nfet_g5v0d10v5 ad=0.25 pd=1.5
+ as=0.25 ps=1.5 w=1 l=3.2
X158 VSS Lower_Nmos_0/IA Lower_Nmos_0/IA VSS sky130_fd_pr__nfet_g5v0d10v5 ad=0.25 pd=1.5 as=0.25
+ ps=1.5 w=1 l=3.2
X159 Lower_Nmos_0/IB Lower_Nmos_0/IA Lower_Nmos_0/IC VSS sky130_fd_pr__nfet_g5v0d10v5 ad=0.25 pd=1.5
+ as=0.25 ps=1.5 w=1 l=3.2
X160 Lower_Nmos_0/IB Lower_Nmos_0/IA Lower_Nmos_0/IC VSS sky130_fd_pr__nfet_g5v0d10v5 ad=0.25 pd=1.5
+ as=0.25 ps=1.5 w=1 l=3.2
X161 Lower_Nmos_0/IC Lower_Nmos_0/IA Lower_Nmos_0/IB VSS sky130_fd_pr__nfet_g5v0d10v5 ad=0.25 pd=1.5
+ as=0.25 ps=1.5 w=1 l=3.2
X162 Lower_Nmos_0/IB Lower_Nmos_0/IA Lower_Nmos_0/IC VSS sky130_fd_pr__nfet_g5v0d10v5 ad=0.25 pd=1.5
+ as=0.25 ps=1.5 w=1 l=3.2
X163 Lower_Nmos_0/IB Lower_Nmos_0/IA Lower_Nmos_0/IC VSS sky130_fd_pr__nfet_g5v0d10v5 ad=0.25 pd=1.5
+ as=0.25 ps=1.5 w=1 l=3.2
X164 Lower_Nmos_0/IC Lower_Nmos_0/IA Lower_Nmos_0/IB VSS sky130_fd_pr__nfet_g5v0d10v5 ad=0.25 pd=1.5
+ as=0.25 ps=1.5 w=1 l=3.2
X165 VSS VSS Lower_Nmos_0/IB VSS sky130_fd_pr__nfet_g5v0d10v5 ad=0.25 pd=1.5 as=0.25 ps=1.5 w=1
+ l=3.2
X166 m1_17410_n5244# VOUT sky130_fd_pr__cap_mim_m3_1 l=8 w=8
X167 m1_17410_n5244# VOUT sky130_fd_pr__cap_mim_m3_1 l=8 w=8
X168 m1_17410_n5244# VOUT sky130_fd_pr__cap_mim_m3_1 l=8 w=8
X169 m1_17410_n5244# VOUT sky130_fd_pr__cap_mim_m3_1 l=8 w=8
C0 m1_17410_n5244# VOUT 29.48602f
C1 Lower_Nmos_0/IC Lower_Nmos_0/IA 4.67946f
C2 VSS Pmos_current_mirror_0/IB 5.40428f
C3 VSS VOUT 5.17316f
C4 VOUT active_load_0/IA 2.72808f
C5 Lower_Nmos_0/IB Lower_Nmos_0/IA 6.14554f
C6 VDD Pmos_current_mirror_0/IC 2.33191f
C7 VSS Lower_Nmos_0/IA 8.39534f
C8 VSS active_load_0/IA 2.70333f
C9 VOUT Pmos_current_mirror_0/IC 5.16991f
C10 Vin+ Vin- 7.8812f
C11 Pmos_current_mirror_0/IA Pmos_current_mirror_0/IC 3.2178f
C12 VSS active_load_0/IB 3.18341f
C13 active_load_0/IB active_load_0/IA 3.94623f
C14 Vin+ Pmos_current_mirror_0/IC 4.40894f
C15 active_load_0/IA Pmos_current_mirror_0/IC 3.7446f
C16 Pmos_current_mirror_0/IB VDD 2.21479f
C17 VOUT VDD 2.66933f
C18 active_load_0/IB Pmos_current_mirror_0/IC 3.62092f
C19 Pmos_current_mirror_0/IB Pmos_current_mirror_0/IA 2.46011f
C20 VDD Pmos_current_mirror_0/IA 42.3693f
C21 Vin- Pmos_current_mirror_0/IC 4.1741f
C22 VOUT Pmos_current_mirror_0/IA 3.75574f
C23 m1_17410_n5244# 0 3.66429f $ **FLOATING
C24 Lower_Nmos_0/IA 0 24.44891f
C25 Lower_Nmos_0/IC 0 2.12289f
C26 VSS 0 27.03676f
C27 Pmos_current_mirror_0/IB 0 11.50098f
C28 VOUT 0 15.46451f
C29 Pmos_current_mirror_0/IA 0 18.95395f
C30 VDD 0 82.29778f
C31 Vin- 0 2.25373f
C32 active_load_0/IA 0 5.84906f
C33 Pmos_current_mirror_0/IC 0 32.86668f
C34 active_load_0/IB 0 8.75947f
.ends


**** end user architecture code
**.ends

* expanding   symbol:  Sky130A/UUT_sky/UUT_VA_sky.sym # of pins=5
** sym_path: my_ip/LIB/Sky130A/UUT_sky/UUT_VA_sky.sym
** sch_path: my_ip/LIB/Sky130A/UUT_sky/UUT_VA_sky.sch
.subckt UUT_VA_sky VDD VSS VIN- VIN+ VOUT
*.iopin VDD
*.iopin VSS
*.iopin VIN-
*.iopin VIN+
*.iopin VOUT
x1 VDD VSS VIN+ VIN- VOUT amplifier
.ends


* expanding   symbol:
*+  Sky130A/Learning/Design_of_Two-Stage_CMOS_Operational_Amplifier_for_Fluorescence_Signal_Processing_5V/amplifier.sym # of pins=5
** sym_path: my_ip/LIB/Sky130A/Learning/Design_of_Two-Stage_CMOS_Operational_Amplifier_for_Fluorescence_Signal_Processing_5V/amplifier.sym
** sch_path: my_ip/LIB/Sky130A/Learning/Design_of_Two-Stage_CMOS_Operational_Amplifier_for_Fluorescence_Signal_Processing_5V/amplifier.sch
.subckt amplifier VDD VSS Vin+ Vin- VOUT
*.iopin VDD
*.iopin VSS
*.iopin Vin+
*.iopin Vin-
*.iopin VOUT
XR2 VSS net2 VSS sky130_fd_pr__res_high_po_0p35 L=20.4 mult=1 m=1
XM7 net1 net1 VSS VSS sky130_fd_pr__nfet_g5v0d10v5 L=3.2 W='1 * 2 ' nf=2 ad='int((nf+1)/2) * W / nf * 0.29'
+ as='int((nf+2)/2) * W / nf * 0.29' pd='2*int((nf+1)/2) * (W / nf + 0.29)' ps='2*int((nf+2)/2) * (W / nf + 0.29)'
+ nrd='0.29 / W ' nrs='0.29 / W ' sa=0 sb=0 sd=0 mult=2 m=2
XM8 net3 net1 net2 VSS sky130_fd_pr__nfet_g5v0d10v5 L=3.2 W='1 * 8 ' nf=8 ad='int((nf+1)/2) * W / nf * 0.29'
+ as='int((nf+2)/2) * W / nf * 0.29' pd='2*int((nf+1)/2) * (W / nf + 0.29)' ps='2*int((nf+2)/2) * (W / nf + 0.29)'
+ nrd='0.29 / W ' nrs='0.29 / W ' sa=0 sb=0 sd=0 mult=2 m=2
XM9 VB1 VB2 net3 VSS sky130_fd_pr__nfet_g5v0d10v5 L=2 W='1 * 2 ' nf=2 ad='int((nf+1)/2) * W / nf * 0.29'
+ as='int((nf+2)/2) * W / nf * 0.29' pd='2*int((nf+1)/2) * (W / nf + 0.29)' ps='2*int((nf+2)/2) * (W / nf + 0.29)'
+ nrd='0.29 / W ' nrs='0.29 / W ' sa=0 sb=0 sd=0 mult=2 m=2
XM10 VB2 VB2 net1 VSS sky130_fd_pr__nfet_g5v0d10v5 L=2 W='1 * 2 ' nf=2 ad='int((nf+1)/2) * W / nf * 0.29'
+ as='int((nf+2)/2) * W / nf * 0.29' pd='2*int((nf+1)/2) * (W / nf + 0.29)' ps='2*int((nf+2)/2) * (W / nf + 0.29)'
+ nrd='0.29 / W ' nrs='0.29 / W ' sa=0 sb=0 sd=0 mult=2 m=2
XM2 net6 Vin- net4 net4 sky130_fd_pr__pfet_g5v0d10v5 L=1 W='4.5 * 2 ' nf=2 ad='int((2 + 1)/2) * 4.5 * 0.29'
+ as='int((2 + 2)/2) * 4.5 * 0.29' pd='2*int((2 + 1)/2) * (4.5 + 0.29)' ps='2*int((2 + 2)/2) * (4.5 + 0.29)'
+ nrd='0.29 / 4.5 / 2 ' nrs='0.29 / 4.5 / 2 ' sa=0 sb=0 sd=0 mult=4 m=4
XM3 net5 Vin+ net4 net4 sky130_fd_pr__pfet_g5v0d10v5 L=1 W='4.5 * 2 ' nf=2 ad='int((2 + 1)/2) * 4.5 * 0.29'
+ as='int((2 + 2)/2) * 4.5 * 0.29' pd='2*int((2 + 1)/2) * (4.5 + 0.29)' ps='2*int((2 + 2)/2) * (4.5 + 0.29)'
+ nrd='0.29 / 4.5 / 2 ' nrs='0.29 / 4.5 / 2 ' sa=0 sb=0 sd=0 mult=4 m=4
XM4 net5 net6 VSS VSS sky130_fd_pr__nfet_g5v0d10v5 L=2 W='1.5 * 2 ' nf=2 ad='int((nf+1)/2) * W / nf * 0.29'
+ as='int((nf+2)/2) * W / nf * 0.29' pd='2*int((nf+1)/2) * (W / nf + 0.29)' ps='2*int((nf+2)/2) * (W / nf + 0.29)'
+ nrd='0.29 / W ' nrs='0.29 / W ' sa=0 sb=0 sd=0 mult=2 m=2
XM11 net6 net6 VSS VSS sky130_fd_pr__nfet_g5v0d10v5 L=2 W='1.5 * 2 ' nf=2 ad='int((nf+1)/2) * W / nf * 0.29'
+ as='int((nf+2)/2) * W / nf * 0.29' pd='2*int((nf+1)/2) * (W / nf + 0.29)' ps='2*int((nf+2)/2) * (W / nf + 0.29)'
+ nrd='0.29 / W ' nrs='0.29 / W ' sa=0 sb=0 sd=0 mult=2 m=2
XM13 VOUT net5 VSS VSS sky130_fd_pr__nfet_g5v0d10v5 L=1 W='4 * 2 ' nf=2 ad='int((nf+1)/2) * W / nf * 0.29'
+ as='int((nf+2)/2) * W / nf * 0.29' pd='2*int((nf+1)/2) * (W / nf + 0.29)' ps='2*int((nf+2)/2) * (W / nf + 0.29)'
+ nrd='0.29 / W ' nrs='0.29 / W ' sa=0 sb=0 sd=0 mult=2 m=2
XM14 net7 VB2 net5 VSS sky130_fd_pr__nfet_g5v0d10v5 L=2 W='1.4 * 1 ' nf=1 ad='int((nf+1)/2) * W / nf * 0.29'
+ as='int((nf+2)/2) * W / nf * 0.29' pd='2*int((nf+1)/2) * (W / nf + 0.29)' ps='2*int((nf+2)/2) * (W / nf + 0.29)'
+ nrd='0.29 / W ' nrs='0.29 / W ' sa=0 sb=0 sd=0 mult=2 m=2
XC1 VOUT net7 sky130_fd_pr__cap_mim_m3_1 W=8 L=8 MF=4 m=4
XM1 VB2 VB1 VDD VDD sky130_fd_pr__pfet_g5v0d10v5 L=2.2 W='1 * 2 ' nf=2 ad='int((2 + 1)/2) * 1 * 0.29'
+ as='int((2 + 2)/2) * 1 * 0.29' pd='2*int((2 + 1)/2) * (1 + 0.29)' ps='2*int((2 + 2)/2) * (1 + 0.29)'
+ nrd='0.29 / 1 / 2 ' nrs='0.29 / 1 / 2 ' sa=0 sb=0 sd=0 mult=2 m=2
XM5 VB1 VB1 VDD VDD sky130_fd_pr__pfet_g5v0d10v5 L=2.2 W='1 * 2 ' nf=2 ad='int((2 + 1)/2) * 1 * 0.29'
+ as='int((2 + 2)/2) * 1 * 0.29' pd='2*int((2 + 1)/2) * (1 + 0.29)' ps='2*int((2 + 2)/2) * (1 + 0.29)'
+ nrd='0.29 / 1 / 2 ' nrs='0.29 / 1 / 2 ' sa=0 sb=0 sd=0 mult=2 m=2
XM6 net4 VB1 VDD VDD sky130_fd_pr__pfet_g5v0d10v5 L=2.2 W='1 * 2 ' nf=2 ad='int((2 + 1)/2) * 1 * 0.29'
+ as='int((2 + 2)/2) * 1 * 0.29' pd='2*int((2 + 1)/2) * (1 + 0.29)' ps='2*int((2 + 2)/2) * (1 + 0.29)'
+ nrd='0.29 / 1 / 2 ' nrs='0.29 / 1 / 2 ' sa=0 sb=0 sd=0 mult=8 m=8
XM12 VOUT VB1 VDD VDD sky130_fd_pr__pfet_g5v0d10v5 L=2.2 W='1 * 2 ' nf=2 ad='int((2 + 1)/2) * 1 * 0.29'
+ as='int((2 + 2)/2) * 1 * 0.29' pd='2*int((2 + 1)/2) * (1 + 0.29)' ps='2*int((2 + 2)/2) * (1 + 0.29)'
+ nrd='0.29 / 1 / 2 ' nrs='0.29 / 1 / 2 ' sa=0 sb=0 sd=0 mult=16 m=16
.ends

.GLOBAL GND
.end
